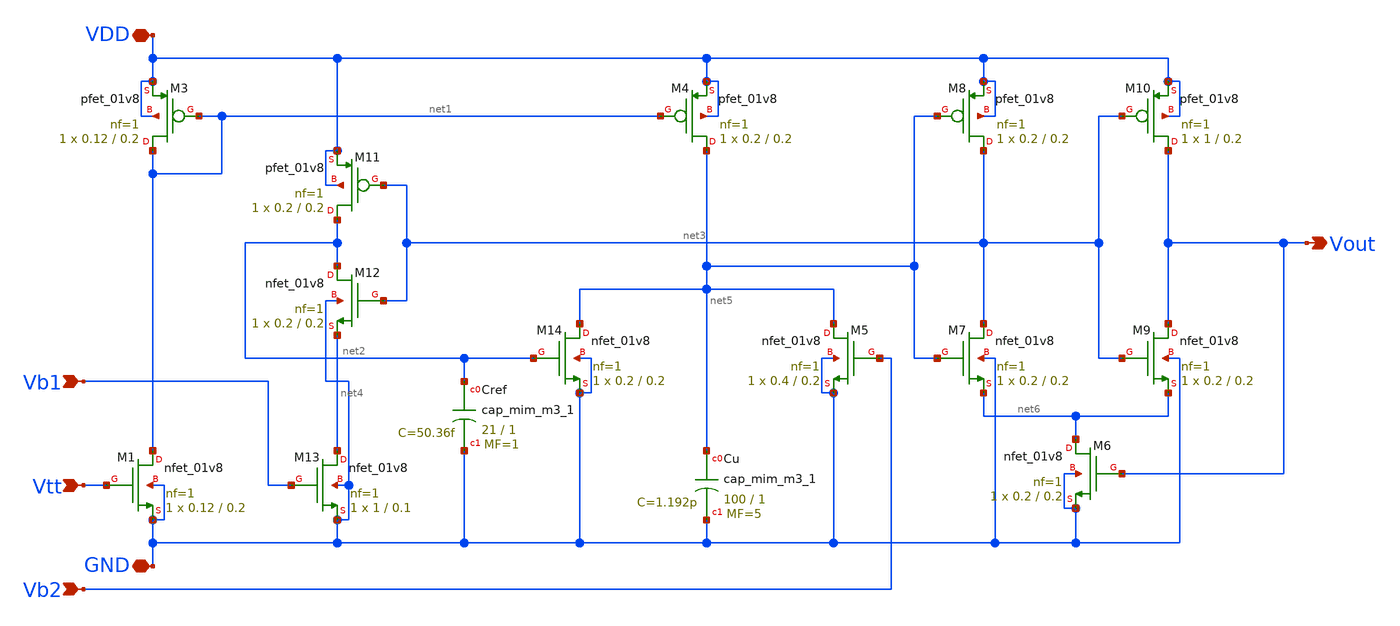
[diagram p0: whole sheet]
** sch_path: LIF_neuron/LIF_neuron_Vohra_original.sch
**.subckt LIF_neuron_Vohra_original Vtt GND Vb1 Vb2 VDD Vout
*.ipin Vtt
*.iopin GND
*.ipin Vb1
*.ipin Vb2
*.iopin VDD
*.opin Vout
XM1 net1 Vtt GND GND sky130_fd_pr__nfet_01v8 L=0.2 W=0.12 nf=1 ad='int((nf+1)/2) * W/nf * 0.29' as='int((nf+2)/2) * W/nf * 0.29'
+ pd='2*int((nf+1)/2) * (W/nf + 0.29)' ps='2*int((nf+2)/2) * (W/nf + 0.29)' nrd='0.29 / W' nrs='0.29 / W'
+ sa=0 sb=0 sd=0 mult=1 m=1
XM3 net1 net1 VDD VDD sky130_fd_pr__pfet_01v8 L=0.2 W=0.12 nf=1 ad='int((nf+1)/2) * W/nf * 0.29' as='int((nf+2)/2) * W/nf * 0.29'
+ pd='2*int((nf+1)/2) * (W/nf + 0.29)' ps='2*int((nf+2)/2) * (W/nf + 0.29)' nrd='0.29 / W' nrs='0.29 / W'
+ sa=0 sb=0 sd=0 mult=1 m=1
XM13 net4 Vb1 GND GND sky130_fd_pr__nfet_01v8 L=0.1 W=1 nf=1 ad='int((nf+1)/2) * W/nf * 0.29' as='int((nf+2)/2) * W/nf * 0.29'
+ pd='2*int((nf+1)/2) * (W/nf + 0.29)' ps='2*int((nf+2)/2) * (W/nf + 0.29)' nrd='0.29 / W' nrs='0.29 / W'
+ sa=0 sb=0 sd=0 mult=1 m=1
XM12 net2 net3 net4 GND sky130_fd_pr__nfet_01v8 L=0.2 W=0.2 nf=1 ad='int((nf+1)/2) * W/nf * 0.29' as='int((nf+2)/2) * W/nf * 0.29'
+ pd='2*int((nf+1)/2) * (W/nf + 0.29)' ps='2*int((nf+2)/2) * (W/nf + 0.29)' nrd='0.29 / W' nrs='0.29 / W'
+ sa=0 sb=0 sd=0 mult=1 m=1
XM11 net2 net3 VDD VDD sky130_fd_pr__pfet_01v8 L=0.2 W=0.2 nf=1 ad='int((nf+1)/2) * W/nf * 0.29' as='int((nf+2)/2) * W/nf * 0.29'
+ pd='2*int((nf+1)/2) * (W/nf + 0.29)' ps='2*int((nf+2)/2) * (W/nf + 0.29)' nrd='0.29 / W' nrs='0.29 / W'
+ sa=0 sb=0 sd=0 mult=1 m=1
XCref net2 GND sky130_fd_pr__cap_mim_m3_1 W=21 L=1 MF=1 m=1
XM14 net5 net2 GND GND sky130_fd_pr__nfet_01v8 L=0.2 W=0.2 nf=1 ad='int((nf+1)/2) * W/nf * 0.29' as='int((nf+2)/2) * W/nf * 0.29'
+ pd='2*int((nf+1)/2) * (W/nf + 0.29)' ps='2*int((nf+2)/2) * (W/nf + 0.29)' nrd='0.29 / W' nrs='0.29 / W'
+ sa=0 sb=0 sd=0 mult=1 m=1
XM4 net5 net1 VDD VDD sky130_fd_pr__pfet_01v8 L=0.2 W=0.2 nf=1 ad='int((nf+1)/2) * W/nf * 0.29' as='int((nf+2)/2) * W/nf * 0.29'
+ pd='2*int((nf+1)/2) * (W/nf + 0.29)' ps='2*int((nf+2)/2) * (W/nf + 0.29)' nrd='0.29 / W' nrs='0.29 / W'
+ sa=0 sb=0 sd=0 mult=1 m=1
XCu net5 GND sky130_fd_pr__cap_mim_m3_1 W=100 L=1 MF=5 m=5
XM5 net5 Vb2 GND GND sky130_fd_pr__nfet_01v8 L=0.2 W=0.4 nf=1 ad='int((nf+1)/2) * W/nf * 0.29' as='int((nf+2)/2) * W/nf * 0.29'
+ pd='2*int((nf+1)/2) * (W/nf + 0.29)' ps='2*int((nf+2)/2) * (W/nf + 0.29)' nrd='0.29 / W' nrs='0.29 / W'
+ sa=0 sb=0 sd=0 mult=1 m=1
XM6 net6 Vout GND GND sky130_fd_pr__nfet_01v8 L=0.2 W=0.2 nf=1 ad='int((nf+1)/2) * W/nf * 0.29' as='int((nf+2)/2) * W/nf * 0.29'
+ pd='2*int((nf+1)/2) * (W/nf + 0.29)' ps='2*int((nf+2)/2) * (W/nf + 0.29)' nrd='0.29 / W' nrs='0.29 / W'
+ sa=0 sb=0 sd=0 mult=1 m=1
XM7 net3 net5 net6 GND sky130_fd_pr__nfet_01v8 L=0.2 W=0.2 nf=1 ad='int((nf+1)/2) * W/nf * 0.29' as='int((nf+2)/2) * W/nf * 0.29'
+ pd='2*int((nf+1)/2) * (W/nf + 0.29)' ps='2*int((nf+2)/2) * (W/nf + 0.29)' nrd='0.29 / W' nrs='0.29 / W'
+ sa=0 sb=0 sd=0 mult=1 m=1
XM8 net3 net5 VDD VDD sky130_fd_pr__pfet_01v8 L=0.2 W=0.2 nf=1 ad='int((nf+1)/2) * W/nf * 0.29' as='int((nf+2)/2) * W/nf * 0.29'
+ pd='2*int((nf+1)/2) * (W/nf + 0.29)' ps='2*int((nf+2)/2) * (W/nf + 0.29)' nrd='0.29 / W' nrs='0.29 / W'
+ sa=0 sb=0 sd=0 mult=1 m=1
XM9 Vout net3 net6 GND sky130_fd_pr__nfet_01v8 L=0.2 W=0.2 nf=1 ad='int((nf+1)/2) * W/nf * 0.29' as='int((nf+2)/2) * W/nf * 0.29'
+ pd='2*int((nf+1)/2) * (W/nf + 0.29)' ps='2*int((nf+2)/2) * (W/nf + 0.29)' nrd='0.29 / W' nrs='0.29 / W'
+ sa=0 sb=0 sd=0 mult=1 m=1
XM10 Vout net3 VDD VDD sky130_fd_pr__pfet_01v8 L=0.2 W=1 nf=1 ad='int((nf+1)/2) * W/nf * 0.29' as='int((nf+2)/2) * W/nf * 0.29'
+ pd='2*int((nf+1)/2) * (W/nf + 0.29)' ps='2*int((nf+2)/2) * (W/nf + 0.29)' nrd='0.29 / W' nrs='0.29 / W'
+ sa=0 sb=0 sd=0 mult=1 m=1
**.ends
.end
